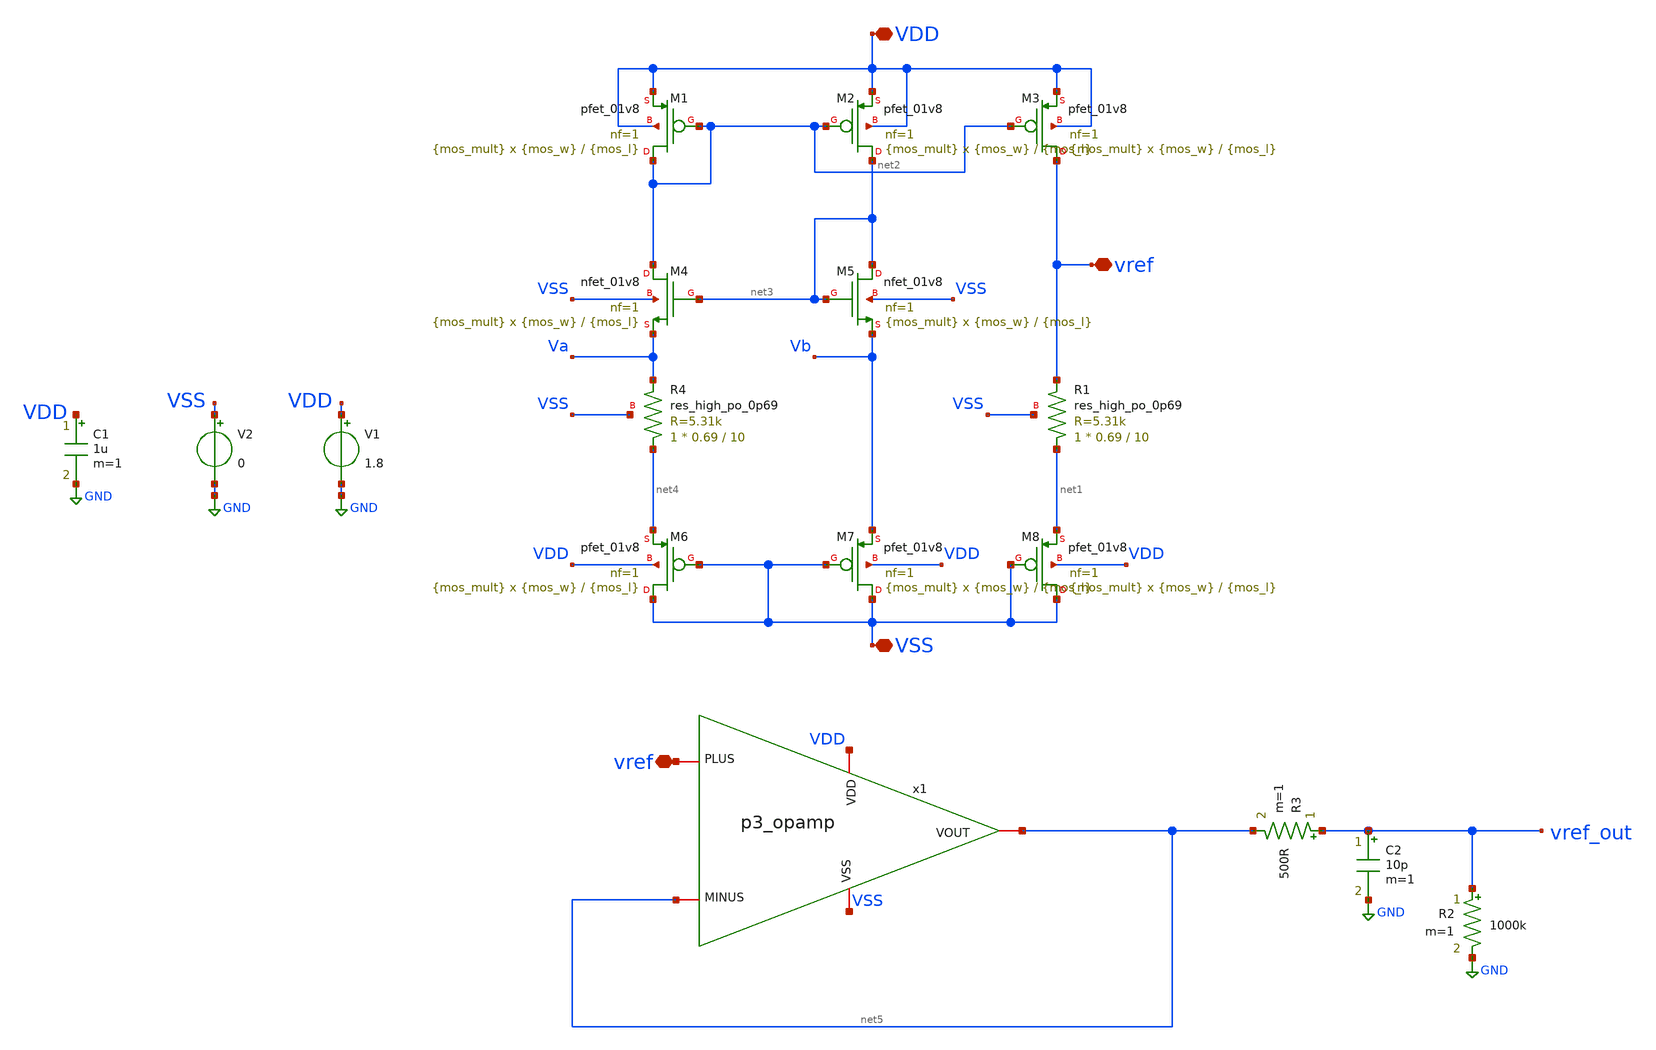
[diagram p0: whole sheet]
** sch_path: xschem/bandgap.sch
**.subckt bandgap VSS VDD vref vref
*.iopin VSS
*.iopin VDD
*.iopin vref
*.iopin vref
XM1 net2 net2 VDD VDD sky130_fd_pr__pfet_01v8 L={mos_l} W={mos_w} nf=1 ad='int((nf+1)/2) * W/nf * 0.29'
+ as='int((nf+2)/2) * W/nf * 0.29' pd='2*int((nf+1)/2) * (W/nf + 0.29)' ps='2*int((nf+2)/2) * (W/nf + 0.29)'
+ nrd='0.29 / W' nrs='0.29 / W' sa=0 sb=0 sd=0 mult={mos_mult} m={mos_mult}
XM2 net3 net2 VDD VDD sky130_fd_pr__pfet_01v8 L={mos_l} W={mos_w} nf=1 ad='int((nf+1)/2) * W/nf * 0.29'
+ as='int((nf+2)/2) * W/nf * 0.29' pd='2*int((nf+1)/2) * (W/nf + 0.29)' ps='2*int((nf+2)/2) * (W/nf + 0.29)'
+ nrd='0.29 / W' nrs='0.29 / W' sa=0 sb=0 sd=0 mult={mos_mult} m={mos_mult}
XM3 vref net2 VDD VDD sky130_fd_pr__pfet_01v8 L={mos_l} W={mos_w} nf=1 ad='int((nf+1)/2) * W/nf * 0.29'
+ as='int((nf+2)/2) * W/nf * 0.29' pd='2*int((nf+1)/2) * (W/nf + 0.29)' ps='2*int((nf+2)/2) * (W/nf + 0.29)'
+ nrd='0.29 / W' nrs='0.29 / W' sa=0 sb=0 sd=0 mult={mos_mult} m={mos_mult}
XM4 net2 net3 Va VSS sky130_fd_pr__nfet_01v8 L={mos_l} W={mos_w} nf=1 ad='int((nf+1)/2) * W/nf * 0.29'
+ as='int((nf+2)/2) * W/nf * 0.29' pd='2*int((nf+1)/2) * (W/nf + 0.29)' ps='2*int((nf+2)/2) * (W/nf + 0.29)'
+ nrd='0.29 / W' nrs='0.29 / W' sa=0 sb=0 sd=0 mult={mos_mult} m={mos_mult}
XM5 net3 net3 Vb VSS sky130_fd_pr__nfet_01v8 L={mos_l} W={mos_w} nf=1 ad='int((nf+1)/2) * W/nf * 0.29'
+ as='int((nf+2)/2) * W/nf * 0.29' pd='2*int((nf+1)/2) * (W/nf + 0.29)' ps='2*int((nf+2)/2) * (W/nf + 0.29)'
+ nrd='0.29 / W' nrs='0.29 / W' sa=0 sb=0 sd=0 mult={mos_mult} m={mos_mult}
XM6 VSS VSS net4 VDD sky130_fd_pr__pfet_01v8 L={mos_l} W={mos_w} nf=1 ad='int((nf+1)/2) * W/nf * 0.29'
+ as='int((nf+2)/2) * W/nf * 0.29' pd='2*int((nf+1)/2) * (W/nf + 0.29)' ps='2*int((nf+2)/2) * (W/nf + 0.29)'
+ nrd='0.29 / W' nrs='0.29 / W' sa=0 sb=0 sd=0 mult={mos_mult} m={mos_mult}
XM7 VSS VSS Vb VDD sky130_fd_pr__pfet_01v8 L={mos_l} W={mos_w} nf=1 ad='int((nf+1)/2) * W/nf * 0.29'
+ as='int((nf+2)/2) * W/nf * 0.29' pd='2*int((nf+1)/2) * (W/nf + 0.29)' ps='2*int((nf+2)/2) * (W/nf + 0.29)'
+ nrd='0.29 / W' nrs='0.29 / W' sa=0 sb=0 sd=0 mult={mos_mult} m={mos_mult}
XM8 VSS VSS net1 VDD sky130_fd_pr__pfet_01v8 L={mos_l} W={mos_w} nf=1 ad='int((nf+1)/2) * W/nf * 0.29'
+ as='int((nf+2)/2) * W/nf * 0.29' pd='2*int((nf+1)/2) * (W/nf + 0.29)' ps='2*int((nf+2)/2) * (W/nf + 0.29)'
+ nrd='0.29 / W' nrs='0.29 / W' sa=0 sb=0 sd=0 mult={mos_mult} m={mos_mult}
V1 VDD GND 1.8
V2 VSS GND 0
XR4 net4 Va VSS sky130_fd_pr__res_high_po_0p69 L=10 mult=1 m=1
XR1 net1 vref VSS sky130_fd_pr__res_high_po_0p69 L=10 mult=1 m=1
x1 VDD net5 vref net5 VSS p3_opamp
C1 VDD GND 1u m=1
R2 vref_out GND 1000k m=1
R3 vref_out net5 500R m=1
C2 vref_out GND 10p m=1
**** begin user architecture code

** opencircuitdesign pdks install
.lib $::SKYWATER_MODELS/sky130.lib.spice tt





*.option  METHOD = GEAR
*.param mc_mm_switch=0
.control
.param mos_mult = 1
.param mos_w = 1
.param mos_l = 0.15
let tempv = 10            ; create a vector vddc and assign 1.8
repeat 20
  set temp = $&tempv         ; alter the voltage V1 using vector vddc
  tran 50p 0.5u uic
  let tempv = tempv + 5   ; update vddc
  write bandgap.raw
  set appendwrite
  reset
end
.endc



**** end user architecture code
**.ends

* expanding   symbol:  p3_opamp.sym # of pins=5
** sym_path: xschem/p3_opamp.sym
** sch_path: xschem/p3_opamp.sch
.subckt p3_opamp VDD MINUS PLUS VOUT VSS
*.iopin VDD
*.iopin VSS
*.iopin PLUS
*.iopin MINUS
*.iopin VOUT
XM3 VX VBIAS VSS VSS sky130_fd_pr__nfet_01v8 L=2 W=4 nf=4 ad='int((nf+1)/2) * W/nf * 0.29' as='int((nf+2)/2) * W/nf * 0.29'
+ pd='2*int((nf+1)/2) * (W/nf + 0.29)' ps='2*int((nf+2)/2) * (W/nf + 0.29)' nrd='0.29 / W' nrs='0.29 / W'
+ sa=0 sb=0 sd=0 mult=1 m=1
XM6 VBIAS VBIAS VSS VSS sky130_fd_pr__nfet_01v8 L=2 W=4 nf=4 ad='int((nf+1)/2) * W/nf * 0.29' as='int((nf+2)/2) * W/nf * 0.29'
+ pd='2*int((nf+1)/2) * (W/nf + 0.29)' ps='2*int((nf+2)/2) * (W/nf + 0.29)' nrd='0.29 / W' nrs='0.29 / W'
+ sa=0 sb=0 sd=0 mult=1 m=1
XM7 VOUT VBIAS VSS VSS sky130_fd_pr__nfet_01v8 L=2 W=7 nf=7 ad='int((nf+1)/2) * W/nf * 0.29' as='int((nf+2)/2) * W/nf * 0.29'
+ pd='2*int((nf+1)/2) * (W/nf + 0.29)' ps='2*int((nf+2)/2) * (W/nf + 0.29)' nrd='0.29 / W' nrs='0.29 / W'
+ sa=0 sb=0 sd=0 mult=1 m=1
XR1 VBIAS VDD VSS sky130_fd_pr__res_xhigh_po_0p35 L=2.8 mult=1 m=1
XM2 V2 MINUS VX VSS sky130_fd_pr__nfet_01v8_lvt L=0.5 W=2.5 nf=1 ad='int((nf+1)/2) * W/nf * 0.29' as='int((nf+2)/2) * W/nf * 0.29'
+ pd='2*int((nf+1)/2) * (W/nf + 0.29)' ps='2*int((nf+2)/2) * (W/nf + 0.29)' nrd='0.29 / W' nrs='0.29 / W'
+ sa=0 sb=0 sd=0 mult=1 m=1
XM1 V1 PLUS VX VSS sky130_fd_pr__nfet_01v8_lvt L=0.5 W=2.5 nf=1 ad='int((nf+1)/2) * W/nf * 0.29' as='int((nf+2)/2) * W/nf * 0.29'
+ pd='2*int((nf+1)/2) * (W/nf + 0.29)' ps='2*int((nf+2)/2) * (W/nf + 0.29)' nrd='0.29 / W' nrs='0.29 / W'
+ sa=0 sb=0 sd=0 mult=1 m=1
XM4 V2 V2 VDD VDD sky130_fd_pr__pfet_01v8_lvt L=2 W=6 nf=6 ad='int((nf+1)/2) * W/nf * 0.29' as='int((nf+2)/2) * W/nf * 0.29'
+ pd='2*int((nf+1)/2) * (W/nf + 0.29)' ps='2*int((nf+2)/2) * (W/nf + 0.29)' nrd='0.29 / W' nrs='0.29 / W'
+ sa=0 sb=0 sd=0 mult=1 m=1
XM5 V1 V2 VDD VDD sky130_fd_pr__pfet_01v8_lvt L=2 W=6 nf=6 ad='int((nf+1)/2) * W/nf * 0.29' as='int((nf+2)/2) * W/nf * 0.29'
+ pd='2*int((nf+1)/2) * (W/nf + 0.29)' ps='2*int((nf+2)/2) * (W/nf + 0.29)' nrd='0.29 / W' nrs='0.29 / W'
+ sa=0 sb=0 sd=0 mult=1 m=1
XM8 VOUT V1 VDD VDD sky130_fd_pr__pfet_01v8_lvt L=0.5 W=20 nf=20 ad='int((nf+1)/2) * W/nf * 0.29' as='int((nf+2)/2) * W/nf * 0.29'
+ pd='2*int((nf+1)/2) * (W/nf + 0.29)' ps='2*int((nf+2)/2) * (W/nf + 0.29)' nrd='0.29 / W' nrs='0.29 / W'
+ sa=0 sb=0 sd=0 mult=1 m=1
.ends

.GLOBAL GND
.end
